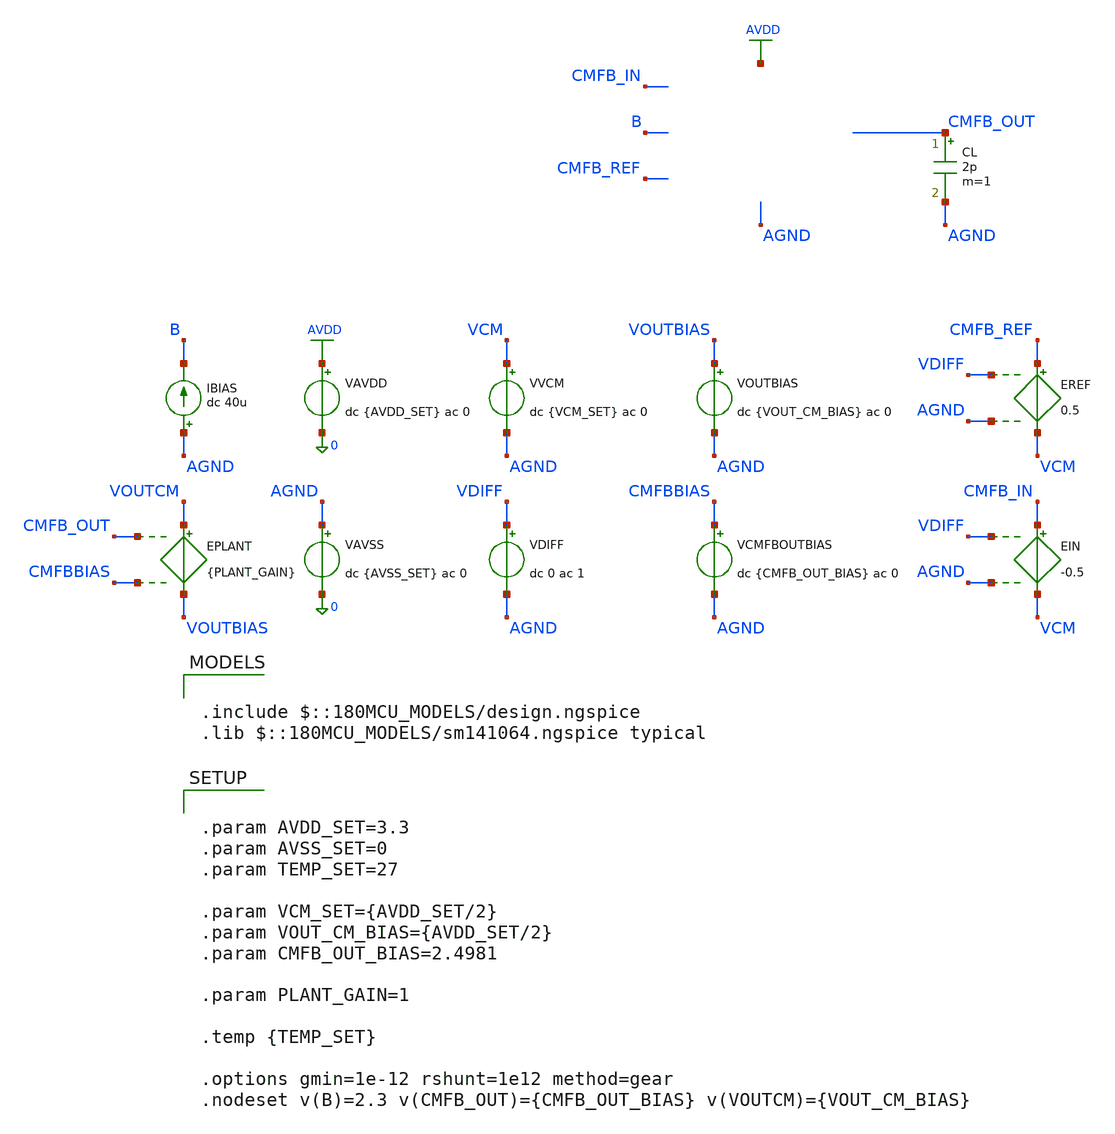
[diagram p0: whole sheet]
** sch_path: Design_Files/IC Design/Testbench/FD_OTA/FDOTA/Open_Loop/FD_OTA_TB_OL_NOM.sch
**.subckt FD_OTA_TB_OL_NOM
IBIAS AGND B dc 40u
VAVDD AVDD 0 dc {AVDD_SET} ac 0
.save i(vavdd)
CL CMFB_OUT AGND 2p m=1
VVCM VCM AGND dc {VCM_SET} ac 0
VDIFF VDIFF AGND dc 0 ac 1
VAVSS AGND 0 dc {AVSS_SET} ac 0
.save i(vavss)
VOUTBIAS VOUTBIAS AGND dc {VOUT_CM_BIAS} ac 0
VCMFBOUTBIAS CMFBBIAS AGND dc {CMFB_OUT_BIAS} ac 0
EREF CMFB_REF VCM VDIFF AGND 0.5
EIN CMFB_IN VCM VDIFF AGND -0.5
EPLANT VOUTCM VOUTBIAS CMFB_OUT CMFBBIAS {PLANT_GAIN}
**** begin user architecture code

.include $::180MCU_MODELS/design.ngspice
.lib $::180MCU_MODELS/sm141064.ngspice typical



.control
destroy all
save all
set wr_vecnames
set wr_singlescale
option numdgt=15

shell mkdir -p
+ /foss/designs/ECG_Acquisition_IC/Measurement_Results/IC_Simulation/FD_OTA/CMFB/NOM.Result_txt

shell rm -f
+ /foss/designs/ECG_Acquisition_IC/Measurement_Results/IC_Simulation/FD_OTA/CMFB/NOM.Result_txt/NOM.ol_ac.txt

let avdd_run = 3.3
let vcm_run  = avdd_run/2

alter @VAVDD[DC] = $&avdd_run
alter @VVCM[DC]  = $&vcm_run
alter @VDIFF[DC] = 0

alter @VVCM[ACMAG]   = 0
alter @VDIFF[ACMAG]  = 1
alter @VDIFF[ACPHASE] = 0
alter @VAVDD[ACMAG]  = 0
alter @VAVSS[ACMAG]  = 0

* Open-loop AC
ac dec 200 1 1G

let error_ac = v(cmfb_ref)-v(cmfb_in)
let loop_ac  = v(voutcm)/error_ac

let loop_real = real(loop_ac)
let loop_imag = imag(loop_ac)

setscale frequency

wrdata
+ /foss/designs/ECG_Acquisition_IC/Measurement_Results/IC_Simulation/FD_OTA/CMFB/NOM.Result_txt/NOM.ol_ac.txt loop_real loop_imag

.endc




.param AVDD_SET=3.3
.param AVSS_SET=0
.param TEMP_SET=27

.param VCM_SET={AVDD_SET/2}
.param VOUT_CM_BIAS={AVDD_SET/2}
.param CMFB_OUT_BIAS=2.4981

.param PLANT_GAIN=1

.temp {TEMP_SET}

.options gmin=1e-12 rshunt=1e12 method=gear
.nodeset v(B)=2.3 v(CMFB_OUT)={CMFB_OUT_BIAS} v(VOUTCM)={VOUT_CM_BIAS}


**** end user architecture code
**.ends
.GLOBAL AVDD
.end
